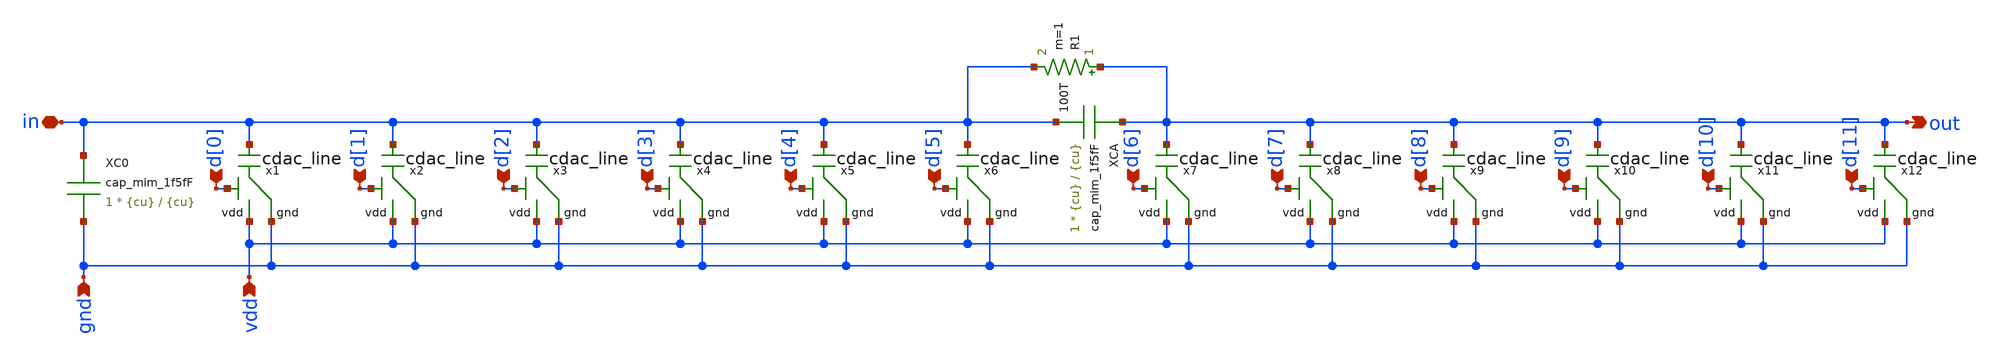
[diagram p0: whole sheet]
** sch_path: symbols/cdac.sch
**.subckt cdac d[0] d[1] d[2] d[3] d[4] d[5] d[6] d[7] d[8] d[9] d[10] d[11] vdd gnd out in
*.ipin d[0]
*.ipin d[1]
*.ipin d[2]
*.ipin d[3]
*.ipin d[4]
*.ipin d[5]
*.ipin d[6]
*.ipin d[7]
*.ipin d[8]
*.ipin d[9]
*.ipin d[10]
*.ipin d[11]
*.ipin vdd
*.ipin gnd
*.opin out
*.iopin in
x1 in vdd gnd d[0] cdac_line CW={sqrt(2)*cu} CL={sqrt(2)*cu}
x2 in vdd gnd d[1] cdac_line CW={sqrt(3)*cu} CL={sqrt(3)*cu}
x3 in vdd gnd d[2] cdac_line CW={sqrt(4)*cu} CL={sqrt(4)*cu}
x4 in vdd gnd d[3] cdac_line CW={sqrt(8)*cu} CL={sqrt(8)*cu}
x5 in vdd gnd d[4] cdac_line CW={sqrt(16)*cu} CL={sqrt(16)*cu}
x6 in vdd gnd d[5] cdac_line CW={sqrt(32)*cu} CL={sqrt(32)*cu}
XCA out in cap_mim_1f5fF c_width={cu} c_length={cu} m=1
x7 out vdd gnd d[6] cdac_line CW={sqrt(1)*cu} CL={sqrt(1)*cu}
x8 out vdd gnd d[7] cdac_line CW={sqrt(2)*cu} CL={sqrt(2)*cu}
x9 out vdd gnd d[8] cdac_line CW={sqrt(4)*cu} CL={sqrt(4)*cu}
x10 out vdd gnd d[9] cdac_line CW={sqrt(8)*cu} CL={sqrt(8)*cu}
x11 out vdd gnd d[10] cdac_line CW={sqrt(16)*cu} CL={sqrt(16)*cu}
x12 out vdd gnd d[11] cdac_line CW={sqrt(32)*cu} CL={sqrt(32)*cu}
R1 out in 100T m=1
XC0 in gnd cap_mim_1f5fF c_width={cu} c_length={cu} m=1
**.ends

* expanding   symbol:  /foss/designs/sar_adc/xschem/spice/cdac_line.sym # of pins=4
** sym_path: /foss/designs/sar_adc/xschem/spice/cdac_line.sym
** sch_path: /foss/designs/sar_adc/xschem/spice/cdac_line.sch
.subckt cdac_line vout vdd gnd vin  CW=1e-6 CL=1e-6
*.ipin vdd
*.ipin gnd
*.ipin vin
*.opin vout
x1 vdd gnd net1 net2 inv cl=0.28u wp=0.66u wn=0.22u
XC1 vout net1 cap_mim_1f5fF c_width=CW c_length=CL m=1
x2 vdd gnd net2 vin inv cl=0.28u wp=0.66u wn=0.22u
.ends


* expanding   symbol:  /foss/designs/sar_adc/xschem/spice/inv.sym # of pins=4
** sym_path: /foss/designs/sar_adc/xschem/spice/inv.sym
** sch_path: /foss/designs/sar_adc/xschem/spice/inv.sch
.subckt inv vdd gnd vout vin  cl=0.28u wp=0.44u wn=0.22u
*.ipin gnd
*.ipin vdd
*.ipin vin
*.opin vout
XM1 gnd vin vout gnd nfet_03v3 L=0.28u W=.22u nf=1 ad='int((nf+1)/2) * W/nf * 0.18u' as='int((nf+2)/2) * W/nf * 0.18u'
+ pd='2*int((nf+1)/2) * (W/nf + 0.18u)' ps='2*int((nf+2)/2) * (W/nf + 0.18u)' nrd='0.18u / W' nrs='0.18u / W'
+ sa=0 sb=0 sd=0 m=1
XM2 vdd vin vout vdd pfet_03v3 L=0.28u W=.22u nf=1 ad='int((nf+1)/2) * W/nf * 0.18u' as='int((nf+2)/2) * W/nf * 0.18u'
+ pd='2*int((nf+1)/2) * (W/nf + 0.18u)' ps='2*int((nf+2)/2) * (W/nf + 0.18u)' nrd='0.18u / W' nrs='0.18u / W'
+ sa=0 sb=0 sd=0 m=1
.ends

.end
